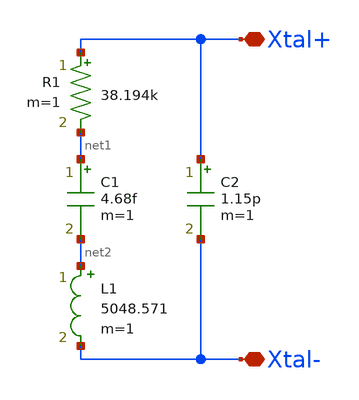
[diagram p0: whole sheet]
** sch_path: design/THESIS_EXP_RO_INVERTER_SKY130A/xtal.sch
**.subckt xtal Xtal+ Xtal-
*.iopin Xtal+
*.iopin Xtal-
R1 Xtal+ net1 38.194k m=1
C1 net1 net2 4.68f m=1
L1 net2 Xtal- 5048.571 m=1
C2 Xtal+ Xtal- 1.15p m=1
**.ends
.end
